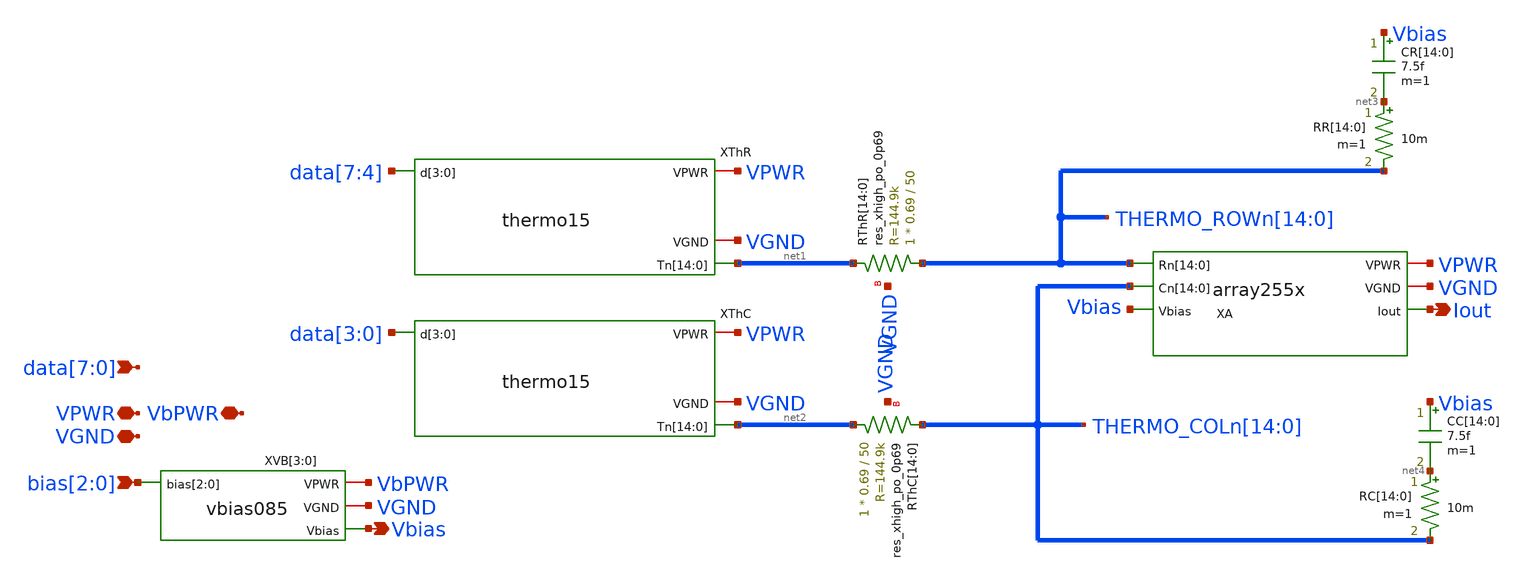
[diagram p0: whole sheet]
** sch_path: xschem/csdac255.sch
**.subckt csdac255 VPWR Iout VGND bias[2],bias[1],bias[0]
*+ data[7],data[6],data[5],data[4],data[3],data[2],data[1],data[0] VbPWR Vbias
*.iopin VPWR
*.opin Iout
*.iopin VGND
*.ipin bias[2],bias[1],bias[0]
*.ipin data[7],data[6],data[5],data[4],data[3],data[2],data[1],data[0]
*.iopin VbPWR
*.opin Vbias
XThR VPWR VGND net1[14] net1[13] net1[12] net1[11] net1[10] net1[9] net1[8] net1[7] net1[6] net1[5]
+ net1[4] net1[3] net1[2] net1[1] net1[0] data[7] data[6] data[5] data[4] thermo15
XA VPWR VGND THERMO_ROWn[14] THERMO_ROWn[13] THERMO_ROWn[12] THERMO_ROWn[11] THERMO_ROWn[10]
+ THERMO_ROWn[9] THERMO_ROWn[8] THERMO_ROWn[7] THERMO_ROWn[6] THERMO_ROWn[5] THERMO_ROWn[4] THERMO_ROWn[3]
+ THERMO_ROWn[2] THERMO_ROWn[1] THERMO_ROWn[0] THERMO_COLn[14] THERMO_COLn[13] THERMO_COLn[12] THERMO_COLn[11]
+ THERMO_COLn[10] THERMO_COLn[9] THERMO_COLn[8] THERMO_COLn[7] THERMO_COLn[6] THERMO_COLn[5] THERMO_COLn[4]
+ THERMO_COLn[3] THERMO_COLn[2] THERMO_COLn[1] THERMO_COLn[0] Vbias Iout array255x
XThC VPWR VGND net2[14] net2[13] net2[12] net2[11] net2[10] net2[9] net2[8] net2[7] net2[6] net2[5]
+ net2[4] net2[3] net2[2] net2[1] net2[0] data[3] data[2] data[1] data[0] thermo15
CR[14] Vbias net3[14] 7.5f m=1
CR[13] Vbias net3[13] 7.5f m=1
CR[12] Vbias net3[12] 7.5f m=1
CR[11] Vbias net3[11] 7.5f m=1
CR[10] Vbias net3[10] 7.5f m=1
CR[9] Vbias net3[9] 7.5f m=1
CR[8] Vbias net3[8] 7.5f m=1
CR[7] Vbias net3[7] 7.5f m=1
CR[6] Vbias net3[6] 7.5f m=1
CR[5] Vbias net3[5] 7.5f m=1
CR[4] Vbias net3[4] 7.5f m=1
CR[3] Vbias net3[3] 7.5f m=1
CR[2] Vbias net3[2] 7.5f m=1
CR[1] Vbias net3[1] 7.5f m=1
CR[0] Vbias net3[0] 7.5f m=1
RR[14] net3[14] THERMO_ROWn[14] 10m m=1
RR[13] net3[13] THERMO_ROWn[13] 10m m=1
RR[12] net3[12] THERMO_ROWn[12] 10m m=1
RR[11] net3[11] THERMO_ROWn[11] 10m m=1
RR[10] net3[10] THERMO_ROWn[10] 10m m=1
RR[9] net3[9] THERMO_ROWn[9] 10m m=1
RR[8] net3[8] THERMO_ROWn[8] 10m m=1
RR[7] net3[7] THERMO_ROWn[7] 10m m=1
RR[6] net3[6] THERMO_ROWn[6] 10m m=1
RR[5] net3[5] THERMO_ROWn[5] 10m m=1
RR[4] net3[4] THERMO_ROWn[4] 10m m=1
RR[3] net3[3] THERMO_ROWn[3] 10m m=1
RR[2] net3[2] THERMO_ROWn[2] 10m m=1
RR[1] net3[1] THERMO_ROWn[1] 10m m=1
RR[0] net3[0] THERMO_ROWn[0] 10m m=1
CC[14] Vbias net4[14] 7.5f m=1
CC[13] Vbias net4[13] 7.5f m=1
CC[12] Vbias net4[12] 7.5f m=1
CC[11] Vbias net4[11] 7.5f m=1
CC[10] Vbias net4[10] 7.5f m=1
CC[9] Vbias net4[9] 7.5f m=1
CC[8] Vbias net4[8] 7.5f m=1
CC[7] Vbias net4[7] 7.5f m=1
CC[6] Vbias net4[6] 7.5f m=1
CC[5] Vbias net4[5] 7.5f m=1
CC[4] Vbias net4[4] 7.5f m=1
CC[3] Vbias net4[3] 7.5f m=1
CC[2] Vbias net4[2] 7.5f m=1
CC[1] Vbias net4[1] 7.5f m=1
CC[0] Vbias net4[0] 7.5f m=1
RC[14] net4[14] THERMO_COLn[14] 10m m=1
RC[13] net4[13] THERMO_COLn[13] 10m m=1
RC[12] net4[12] THERMO_COLn[12] 10m m=1
RC[11] net4[11] THERMO_COLn[11] 10m m=1
RC[10] net4[10] THERMO_COLn[10] 10m m=1
RC[9] net4[9] THERMO_COLn[9] 10m m=1
RC[8] net4[8] THERMO_COLn[8] 10m m=1
RC[7] net4[7] THERMO_COLn[7] 10m m=1
RC[6] net4[6] THERMO_COLn[6] 10m m=1
RC[5] net4[5] THERMO_COLn[5] 10m m=1
RC[4] net4[4] THERMO_COLn[4] 10m m=1
RC[3] net4[3] THERMO_COLn[3] 10m m=1
RC[2] net4[2] THERMO_COLn[2] 10m m=1
RC[1] net4[1] THERMO_COLn[1] 10m m=1
RC[0] net4[0] THERMO_COLn[0] 10m m=1
XVB[3] VbPWR VGND bias[2] bias[1] bias[0] Vbias vbias085
XVB[2] VbPWR VGND bias[2] bias[1] bias[0] Vbias vbias085
XVB[1] VbPWR VGND bias[2] bias[1] bias[0] Vbias vbias085
XVB[0] VbPWR VGND bias[2] bias[1] bias[0] Vbias vbias085
XRThR[14] THERMO_ROWn[14] net1[14] VGND sky130_fd_pr__res_xhigh_po_0p69 L=50 mult=1 m=1
XRThR[13] THERMO_ROWn[13] net1[13] VGND sky130_fd_pr__res_xhigh_po_0p69 L=50 mult=1 m=1
XRThR[12] THERMO_ROWn[12] net1[12] VGND sky130_fd_pr__res_xhigh_po_0p69 L=50 mult=1 m=1
XRThR[11] THERMO_ROWn[11] net1[11] VGND sky130_fd_pr__res_xhigh_po_0p69 L=50 mult=1 m=1
XRThR[10] THERMO_ROWn[10] net1[10] VGND sky130_fd_pr__res_xhigh_po_0p69 L=50 mult=1 m=1
XRThR[9] THERMO_ROWn[9] net1[9] VGND sky130_fd_pr__res_xhigh_po_0p69 L=50 mult=1 m=1
XRThR[8] THERMO_ROWn[8] net1[8] VGND sky130_fd_pr__res_xhigh_po_0p69 L=50 mult=1 m=1
XRThR[7] THERMO_ROWn[7] net1[7] VGND sky130_fd_pr__res_xhigh_po_0p69 L=50 mult=1 m=1
XRThR[6] THERMO_ROWn[6] net1[6] VGND sky130_fd_pr__res_xhigh_po_0p69 L=50 mult=1 m=1
XRThR[5] THERMO_ROWn[5] net1[5] VGND sky130_fd_pr__res_xhigh_po_0p69 L=50 mult=1 m=1
XRThR[4] THERMO_ROWn[4] net1[4] VGND sky130_fd_pr__res_xhigh_po_0p69 L=50 mult=1 m=1
XRThR[3] THERMO_ROWn[3] net1[3] VGND sky130_fd_pr__res_xhigh_po_0p69 L=50 mult=1 m=1
XRThR[2] THERMO_ROWn[2] net1[2] VGND sky130_fd_pr__res_xhigh_po_0p69 L=50 mult=1 m=1
XRThR[1] THERMO_ROWn[1] net1[1] VGND sky130_fd_pr__res_xhigh_po_0p69 L=50 mult=1 m=1
XRThR[0] THERMO_ROWn[0] net1[0] VGND sky130_fd_pr__res_xhigh_po_0p69 L=50 mult=1 m=1
XRThC[14] net2[14] THERMO_COLn[14] VGND sky130_fd_pr__res_xhigh_po_0p69 L=50 mult=1 m=1
XRThC[13] net2[13] THERMO_COLn[13] VGND sky130_fd_pr__res_xhigh_po_0p69 L=50 mult=1 m=1
XRThC[12] net2[12] THERMO_COLn[12] VGND sky130_fd_pr__res_xhigh_po_0p69 L=50 mult=1 m=1
XRThC[11] net2[11] THERMO_COLn[11] VGND sky130_fd_pr__res_xhigh_po_0p69 L=50 mult=1 m=1
XRThC[10] net2[10] THERMO_COLn[10] VGND sky130_fd_pr__res_xhigh_po_0p69 L=50 mult=1 m=1
XRThC[9] net2[9] THERMO_COLn[9] VGND sky130_fd_pr__res_xhigh_po_0p69 L=50 mult=1 m=1
XRThC[8] net2[8] THERMO_COLn[8] VGND sky130_fd_pr__res_xhigh_po_0p69 L=50 mult=1 m=1
XRThC[7] net2[7] THERMO_COLn[7] VGND sky130_fd_pr__res_xhigh_po_0p69 L=50 mult=1 m=1
XRThC[6] net2[6] THERMO_COLn[6] VGND sky130_fd_pr__res_xhigh_po_0p69 L=50 mult=1 m=1
XRThC[5] net2[5] THERMO_COLn[5] VGND sky130_fd_pr__res_xhigh_po_0p69 L=50 mult=1 m=1
XRThC[4] net2[4] THERMO_COLn[4] VGND sky130_fd_pr__res_xhigh_po_0p69 L=50 mult=1 m=1
XRThC[3] net2[3] THERMO_COLn[3] VGND sky130_fd_pr__res_xhigh_po_0p69 L=50 mult=1 m=1
XRThC[2] net2[2] THERMO_COLn[2] VGND sky130_fd_pr__res_xhigh_po_0p69 L=50 mult=1 m=1
XRThC[1] net2[1] THERMO_COLn[1] VGND sky130_fd_pr__res_xhigh_po_0p69 L=50 mult=1 m=1
XRThC[0] net2[0] THERMO_COLn[0] VGND sky130_fd_pr__res_xhigh_po_0p69 L=50 mult=1 m=1
**.ends
.end
